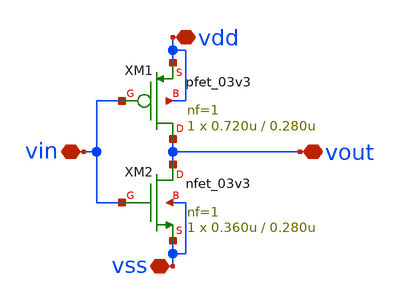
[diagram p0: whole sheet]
** sch_path: test-inv/schematics/inv.sch

.include $env(PDK_ROOT)/$env(PDK)/libs.tech/ngspice/design.ngspice

.lib $env(PDK_ROOT)/$env(PDK)/libs.tech/ngspice/sm141064.ngspice typical
.lib $env(PDK_ROOT)/$env(PDK)/libs.tech/ngspice/sm141064.ngspice mimcap_statistical
.lib $env(PDK_ROOT)/$env(PDK)/libs.tech/ngspice/sm141064.ngspice cap_mim
.lib $env(PDK_ROOT)/$env(PDK)/libs.tech/ngspice/sm141064.ngspice res_typical
.lib $env(PDK_ROOT)/$env(PDK)/libs.tech/ngspice/sm141064.ngspice bjt_typical
.lib $env(PDK_ROOT)/$env(PDK)/libs.tech/ngspice/sm141064.ngspice moscap_typical


**.subckt inv vout vdd vin vss
*.iopin vout
*.iopin vdd
*.iopin vin
*.iopin vss
XM1 vout vin vdd vdd pfet_03v3 L=0.280u W=0.720u nf=1 ad='int((nf+1)/2) * W/nf * 0.18u' as='int((nf+2)/2) * W/nf * 0.18u'
+ pd='2*int((nf+1)/2) * (W/nf + 0.18u)' ps='2*int((nf+2)/2) * (W/nf + 0.18u)' nrd='0.18u / W' nrs='0.18u / W'
+ sa=0 sb=0 sd=0 m=1
XM2 vout vin vss vss nfet_03v3 L=0.280u W=0.360u nf=1 ad='int((nf+1)/2) * W/nf * 0.18u' as='int((nf+2)/2) * W/nf * 0.18u'
+ pd='2*int((nf+1)/2) * (W/nf + 0.18u)' ps='2*int((nf+2)/2) * (W/nf + 0.18u)' nrd='0.18u / W' nrs='0.18u / W'
+ sa=0 sb=0 sd=0 m=1
**.ends
.end
